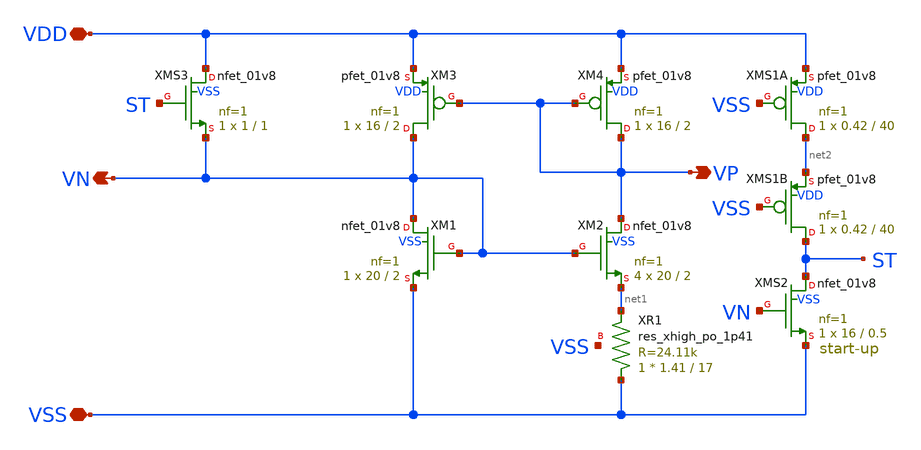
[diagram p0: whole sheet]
** sch_path: xschem/bias_ref.sch
**.subckt bias_ref VP VN VDD VSS
*.opin VP
*.opin VN
*.iopin VDD
*.iopin VSS
XXM3 VN VP VDD VDD sky130_fd_pr__pfet_01v8 L=2 W=16 nf=1 ad='int((1 + 1)/2) * 16 / 1 * 0.29' as='int((1 + 2)/2) * 16 / 1 * 0.29'
+ pd='2*int((1 + 1)/2) * (16 / 1 + 0.29)' ps='2*int((1 + 2)/2) * (16 / 1 + 0.29)' nrd='0.29 / 16 ' nrs='0.29 / 16 '
+ sa=0 sb=0 sd=0 mult=1 m=1
XXM4 VP VP VDD VDD sky130_fd_pr__pfet_01v8 L=2 W=16 nf=1 ad='int((1 + 1)/2) * 16 / 1 * 0.29' as='int((1 + 2)/2) * 16 / 1 * 0.29'
+ pd='2*int((1 + 1)/2) * (16 / 1 + 0.29)' ps='2*int((1 + 2)/2) * (16 / 1 + 0.29)' nrd='0.29 / 16 ' nrs='0.29 / 16 '
+ sa=0 sb=0 sd=0 mult=1 m=1
XXM1 VN VN VSS VSS sky130_fd_pr__nfet_01v8 L=2 W=20 nf=1 ad='int((nf+1)/2) * W/nf * 0.29' as='int((nf+2)/2) * W/nf * 0.29'
+ pd='2*int((nf+1)/2) * (W/nf + 0.29)' ps='2*int((nf+2)/2) * (W/nf + 0.29)' nrd='0.29 / W' nrs='0.29 / W'
+ sa=0 sb=0 sd=0 mult=1 m=1
XXM2 VP VN net1 VSS sky130_fd_pr__nfet_01v8 L=2 W=20 nf=1 ad='int((nf+1)/2) * W/nf * 0.29' as='int((nf+2)/2) * W/nf * 0.29'
+ pd='2*int((nf+1)/2) * (W/nf + 0.29)' ps='2*int((nf+2)/2) * (W/nf + 0.29)' nrd='0.29 / W' nrs='0.29 / W'
+ sa=0 sb=0 sd=0 mult=4 m=4
XXR1 VSS net1 VSS sky130_fd_pr__res_xhigh_po_1p41 L=17 mult=1 m=1
XXMS1A net2 VSS VDD VDD sky130_fd_pr__pfet_01v8 L=40 W=0.42 nf=1 ad='int((1 + 1)/2) * 0.42 / 1 * 0.29'
+ as='int((1 + 2)/2) * 0.42 / 1 * 0.29' pd='2*int((1 + 1)/2) * (0.42 / 1 + 0.29)' ps='2*int((1 + 2)/2) * (0.42 / 1 + 0.29)'
+ nrd='0.29 / 0.42 ' nrs='0.29 / 0.42 ' sa=0 sb=0 sd=0 mult=1 m=1
XXMS1B ST VSS net2 VDD sky130_fd_pr__pfet_01v8 L=40 W=0.42 nf=1 ad='int((1 + 1)/2) * 0.42 / 1 * 0.29'
+ as='int((1 + 2)/2) * 0.42 / 1 * 0.29' pd='2*int((1 + 1)/2) * (0.42 / 1 + 0.29)' ps='2*int((1 + 2)/2) * (0.42 / 1 + 0.29)'
+ nrd='0.29 / 0.42 ' nrs='0.29 / 0.42 ' sa=0 sb=0 sd=0 mult=1 m=1
XXMS2 ST VN VSS VSS sky130_fd_pr__nfet_01v8 L=0.5 W=16 nf=1 ad='int((nf+1)/2) * W/nf * 0.29' as='int((nf+2)/2) * W/nf * 0.29'
+ pd='2*int((nf+1)/2) * (W/nf + 0.29)' ps='2*int((nf+2)/2) * (W/nf + 0.29)' nrd='0.29 / W' nrs='0.29 / W'
+ sa=0 sb=0 sd=0 mult=1 m=1
XXMS3 VDD ST VN VSS sky130_fd_pr__nfet_01v8 L=1 W=1 nf=1 ad='int((nf+1)/2) * W/nf * 0.29' as='int((nf+2)/2) * W/nf * 0.29'
+ pd='2*int((nf+1)/2) * (W/nf + 0.29)' ps='2*int((nf+2)/2) * (W/nf + 0.29)' nrd='0.29 / W' nrs='0.29 / W'
+ sa=0 sb=0 sd=0 mult=1 m=1
**.ends
.end
